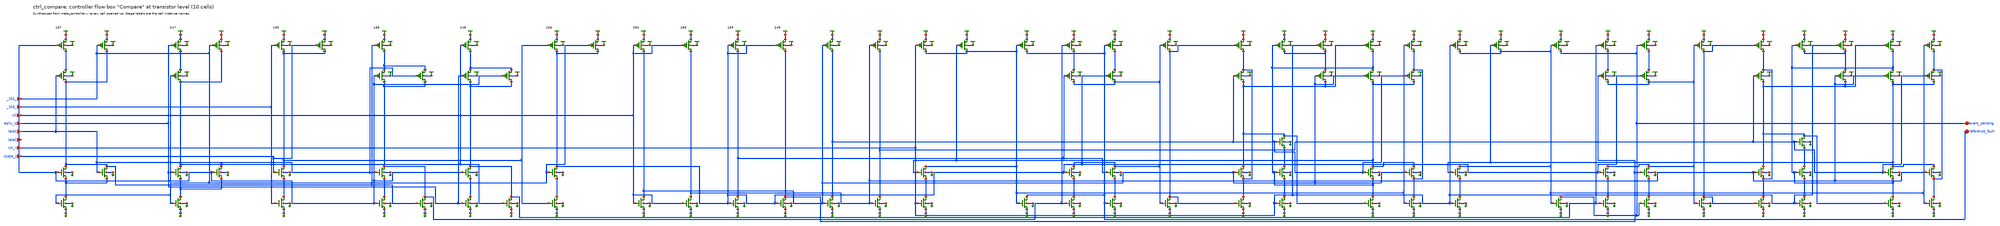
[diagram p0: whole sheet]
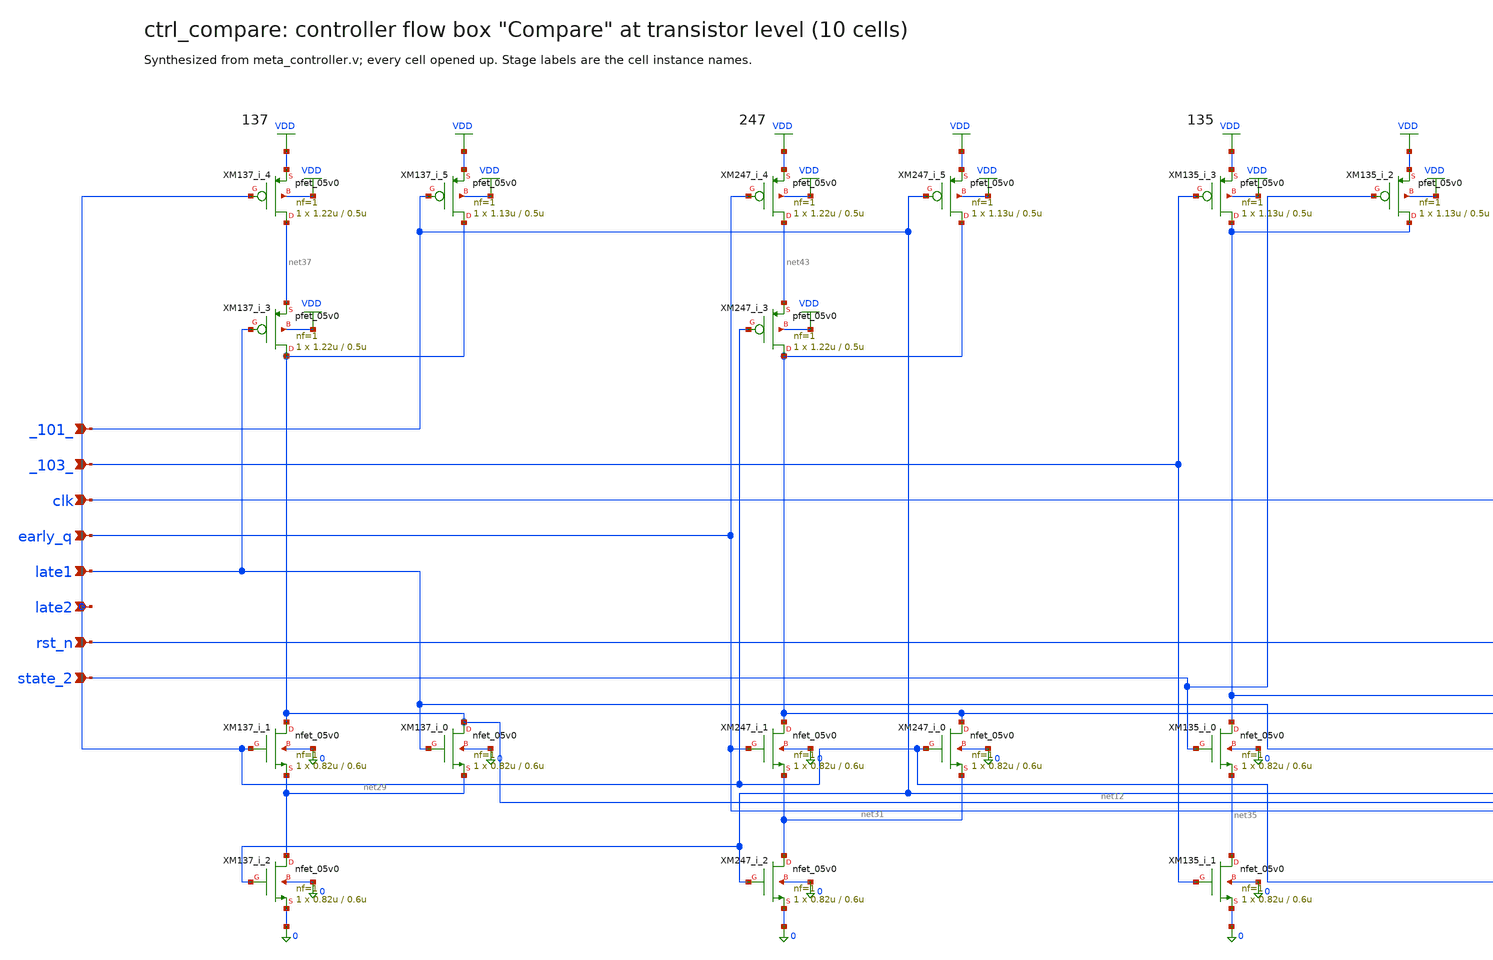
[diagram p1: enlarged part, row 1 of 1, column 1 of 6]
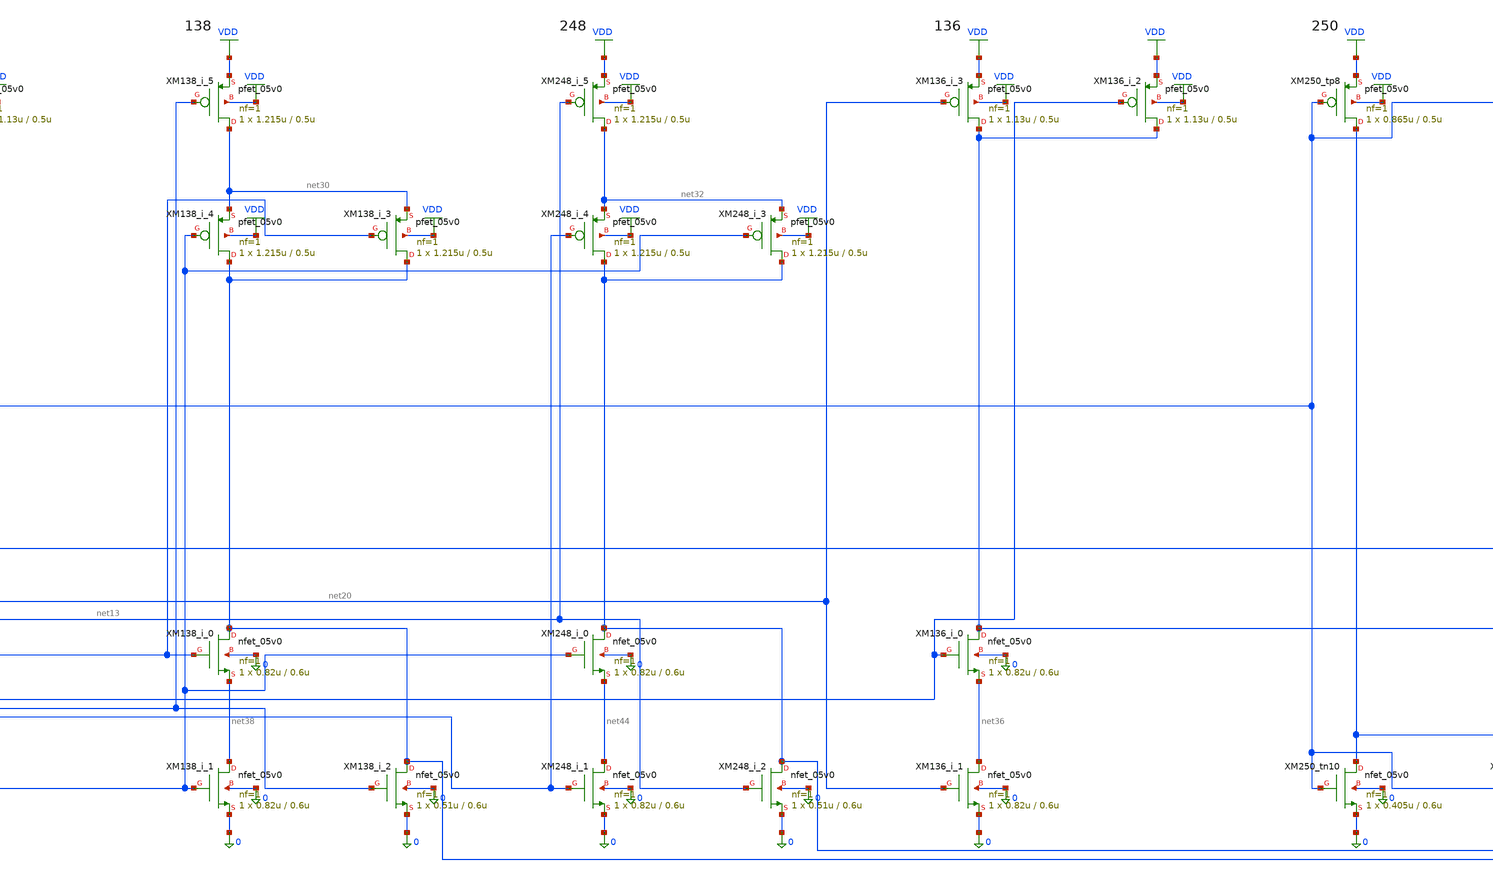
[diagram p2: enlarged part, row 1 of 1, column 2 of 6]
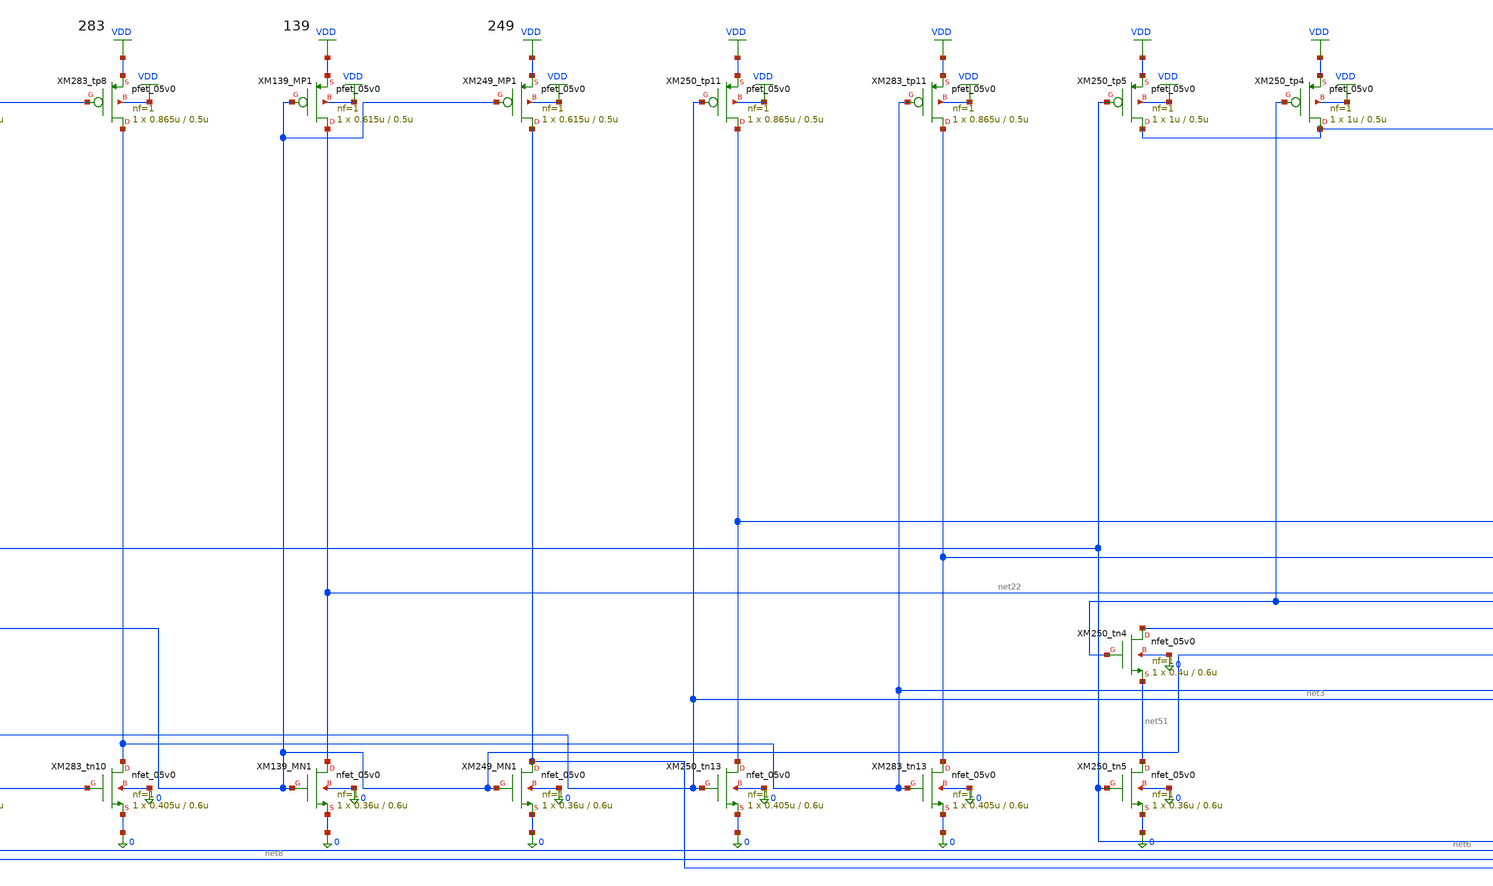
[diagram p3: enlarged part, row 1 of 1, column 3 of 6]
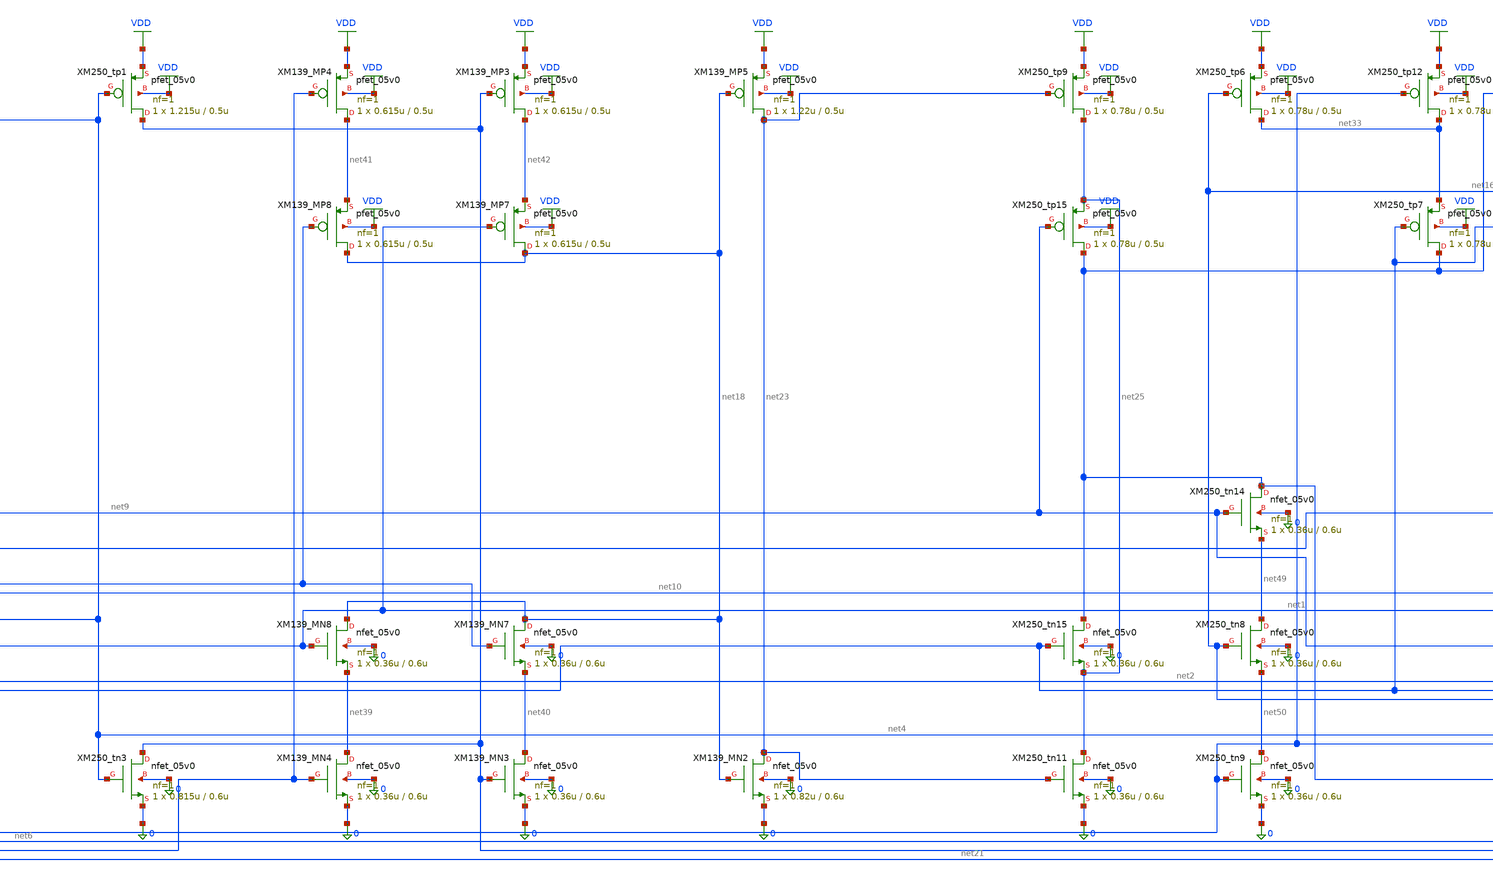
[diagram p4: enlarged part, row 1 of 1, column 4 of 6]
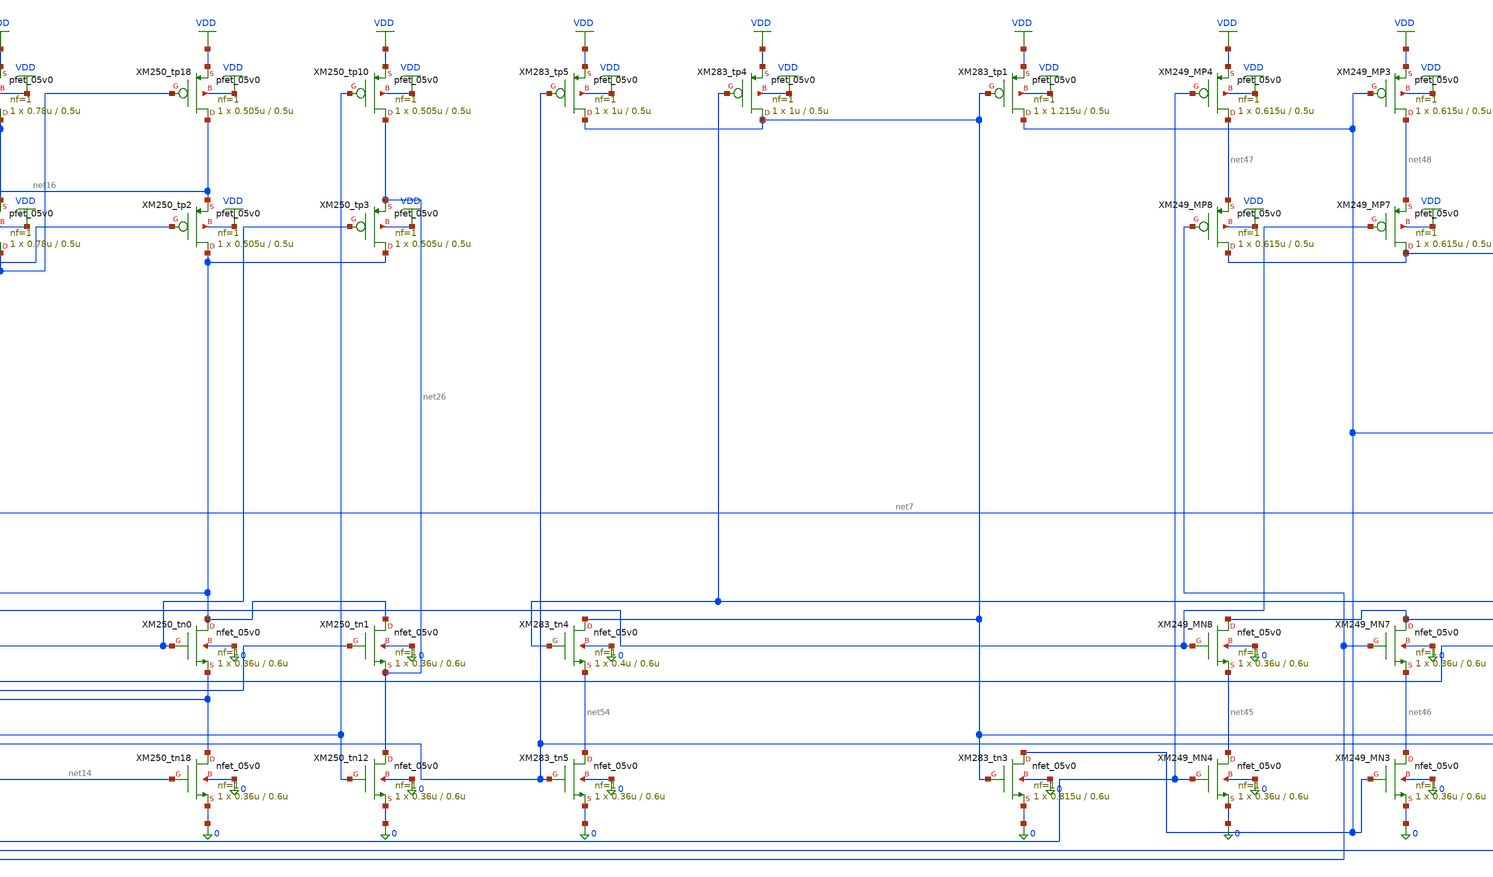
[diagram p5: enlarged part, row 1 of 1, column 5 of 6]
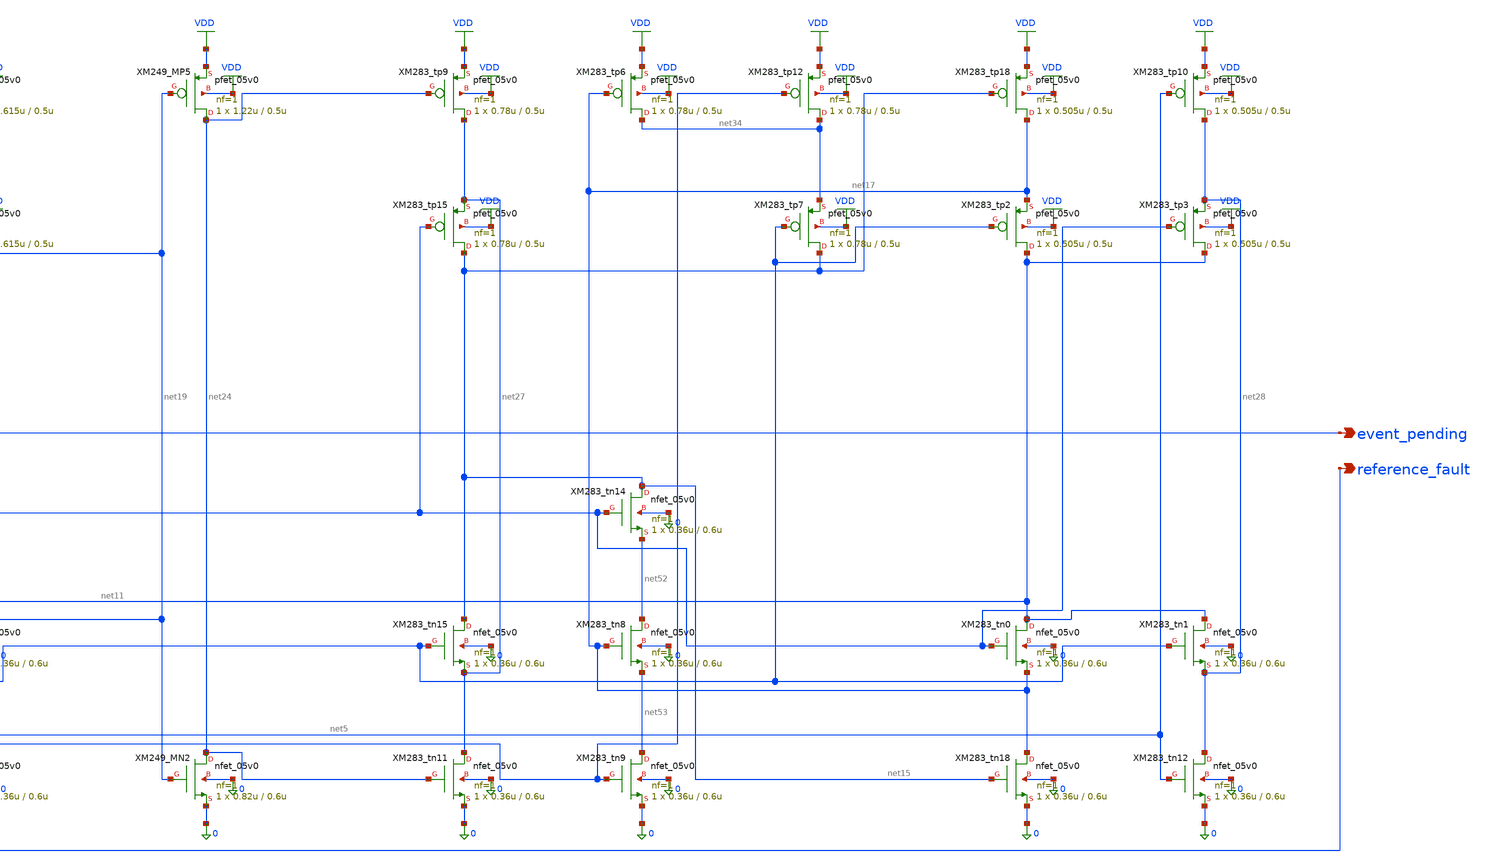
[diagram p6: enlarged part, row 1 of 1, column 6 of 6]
** sch_path: xschem/flat/ctrl_compare.sch
**.subckt ctrl_compare _101_ _103_ clk early_q late1 late2 rst_n state_2 event_pending
*+ reference_fault
*.ipin _101_
*.ipin _103_
*.ipin clk
*.ipin early_q
*.ipin late1
*.ipin late2
*.ipin rst_n
*.ipin state_2
*.opin event_pending
*.opin reference_fault
XM135_i_1 net35 _103_ 0 0 nfet_05v0 L=0.6u W=0.82u nf=1 ad=4.1e-13 as=4.1e-13 pd=2.64e-06
+ ps=2.64e-06 nrd=0 nrs=0 sa=0 sb=0 sd=0 m=1
XM135_i_0 net20 state_2 net35 0 nfet_05v0 L=0.6u W=0.82u nf=1 ad=4.1e-13 as=4.1e-13 pd=2.64e-06
+ ps=2.64e-06 nrd=0 nrs=0 sa=0 sb=0 sd=0 m=1
XM135_i_3 net20 _103_ VDD VDD pfet_05v0 L=0.5u W=1.13u nf=1 ad=5.65e-13 as=5.65e-13 pd=3.26e-06
+ ps=3.26e-06 nrd=0 nrs=0 sa=0 sb=0 sd=0 m=1
XM135_i_2 net20 state_2 VDD VDD pfet_05v0 L=0.5u W=1.13u nf=1 ad=5.65e-13 as=5.65e-13 pd=3.26e-06
+ ps=3.26e-06 nrd=0 nrs=0 sa=0 sb=0 sd=0 m=1
XM136_i_1 net36 net20 0 0 nfet_05v0 L=0.6u W=0.82u nf=1 ad=4.1e-13 as=4.1e-13 pd=2.64e-06
+ ps=2.64e-06 nrd=0 nrs=0 sa=0 sb=0 sd=0 m=1
XM136_i_0 net1 _101_ net36 0 nfet_05v0 L=0.6u W=0.82u nf=1 ad=4.1e-13 as=4.1e-13 pd=2.64e-06
+ ps=2.64e-06 nrd=0 nrs=0 sa=0 sb=0 sd=0 m=1
XM136_i_3 net1 net20 VDD VDD pfet_05v0 L=0.5u W=1.13u nf=1 ad=5.65e-13 as=5.65e-13 pd=3.26e-06
+ ps=3.26e-06 nrd=0 nrs=0 sa=0 sb=0 sd=0 m=1
XM136_i_2 net1 _101_ VDD VDD pfet_05v0 L=0.5u W=1.13u nf=1 ad=5.65e-13 as=5.65e-13 pd=3.26e-06
+ ps=3.26e-06 nrd=0 nrs=0 sa=0 sb=0 sd=0 m=1
XM137_i_1 net12 late2 net29 0 nfet_05v0 L=0.6u W=0.82u nf=1 ad=4.1e-13 as=4.1e-13 pd=2.64e-06
+ ps=2.64e-06 nrd=0 nrs=0 sa=0 sb=0 sd=0 m=1
XM137_i_0 net12 late1 net29 0 nfet_05v0 L=0.6u W=0.82u nf=1 ad=4.1e-13 as=4.1e-13 pd=2.64e-06
+ ps=2.64e-06 nrd=0 nrs=0 sa=0 sb=0 sd=0 m=1
XM137_i_2 net29 _101_ 0 0 nfet_05v0 L=0.6u W=0.82u nf=1 ad=4.1e-13 as=4.1e-13 pd=2.64e-06
+ ps=2.64e-06 nrd=0 nrs=0 sa=0 sb=0 sd=0 m=1
XM137_i_4 net37 late2 VDD VDD pfet_05v0 L=0.5u W=1.22u nf=1 ad=6.1e-13 as=6.1e-13 pd=3.44e-06
+ ps=3.44e-06 nrd=0 nrs=0 sa=0 sb=0 sd=0 m=1
XM137_i_3 net12 late1 net37 VDD pfet_05v0 L=0.5u W=1.22u nf=1 ad=6.1e-13 as=6.1e-13 pd=3.44e-06
+ ps=3.44e-06 nrd=0 nrs=0 sa=0 sb=0 sd=0 m=1
XM137_i_5 net12 _101_ VDD VDD pfet_05v0 L=0.5u W=1.13u nf=1 ad=5.65e-13 as=5.65e-13 pd=3.26e-06
+ ps=3.26e-06 nrd=0 nrs=0 sa=0 sb=0 sd=0 m=1
XM138_i_1 net38 late2 0 0 nfet_05v0 L=0.6u W=0.82u nf=1 ad=4.1e-13 as=4.1e-13 pd=2.64e-06
+ ps=2.64e-06 nrd=0 nrs=0 sa=0 sb=0 sd=0 m=1
XM138_i_0 net8 late1 net38 0 nfet_05v0 L=0.6u W=0.82u nf=1 ad=4.1e-13 as=4.1e-13 pd=2.64e-06
+ ps=2.64e-06 nrd=0 nrs=0 sa=0 sb=0 sd=0 m=1
XM138_i_2 net8 net12 0 0 nfet_05v0 L=0.6u W=0.51u nf=1 ad=2.55e-13 as=2.55e-13 pd=2.02e-06
+ ps=2.02e-06 nrd=0 nrs=0 sa=0 sb=0 sd=0 m=1
XM138_i_4 net8 late2 net30 VDD pfet_05v0 L=0.5u W=1.215u nf=1 ad=6.075e-13 as=6.075e-13 pd=3.43e-06
+ ps=3.43e-06 nrd=0 nrs=0 sa=0 sb=0 sd=0 m=1
XM138_i_3 net8 late1 net30 VDD pfet_05v0 L=0.5u W=1.215u nf=1 ad=6.075e-13 as=6.075e-13 pd=3.43e-06
+ ps=3.43e-06 nrd=0 nrs=0 sa=0 sb=0 sd=0 m=1
XM138_i_5 net30 net12 VDD VDD pfet_05v0 L=0.5u W=1.215u nf=1 ad=6.075e-13 as=6.075e-13 pd=3.43e-06
+ ps=3.43e-06 nrd=0 nrs=0 sa=0 sb=0 sd=0 m=1
XM139_MN2 net23 net18 0 0 nfet_05v0 L=0.6u W=0.82u nf=1 ad=4.1e-13 as=4.1e-13 pd=2.64e-06
+ ps=2.64e-06 nrd=0 nrs=0 sa=0 sb=0 sd=0 m=1
XM139_MN4 net39 net8 0 0 nfet_05v0 L=0.6u W=0.36u nf=1 ad=1.8e-13 as=1.8e-13 pd=1.72e-06 ps=1.72e-06
+ nrd=0 nrs=0 sa=0 sb=0 sd=0 m=1
XM139_MN8 net18 net1 net39 0 nfet_05v0 L=0.6u W=0.36u nf=1 ad=1.8e-13 as=1.8e-13 pd=1.72e-06
+ ps=1.72e-06 nrd=0 nrs=0 sa=0 sb=0 sd=0 m=1
XM139_MN7 net18 net22 net40 0 nfet_05v0 L=0.6u W=0.36u nf=1 ad=1.8e-13 as=1.8e-13 pd=1.72e-06
+ ps=1.72e-06 nrd=0 nrs=0 sa=0 sb=0 sd=0 m=1
XM139_MN3 net40 reference_fault 0 0 nfet_05v0 L=0.6u W=0.36u nf=1 ad=1.8e-13 as=1.8e-13 pd=1.72e-06
+ ps=1.72e-06 nrd=0 nrs=0 sa=0 sb=0 sd=0 m=1
XM139_MN1 net22 net1 0 0 nfet_05v0 L=0.6u W=0.36u nf=1 ad=1.8e-13 as=1.8e-13 pd=1.72e-06 ps=1.72e-06
+ nrd=0 nrs=0 sa=0 sb=0 sd=0 m=1
XM139_MP5 net23 net18 VDD VDD pfet_05v0 L=0.5u W=1.22u nf=1 ad=6.1e-13 as=6.1e-13 pd=3.44e-06
+ ps=3.44e-06 nrd=0 nrs=0 sa=0 sb=0 sd=0 m=1
XM139_MP4 net41 net8 VDD VDD pfet_05v0 L=0.5u W=0.615u nf=1 ad=3.075e-13 as=3.075e-13 pd=2.23e-06
+ ps=2.23e-06 nrd=0 nrs=0 sa=0 sb=0 sd=0 m=1
XM139_MP8 net18 net22 net41 VDD pfet_05v0 L=0.5u W=0.615u nf=1 ad=3.075e-13 as=3.075e-13 pd=2.23e-06
+ ps=2.23e-06 nrd=0 nrs=0 sa=0 sb=0 sd=0 m=1
XM139_MP7 net18 net1 net42 VDD pfet_05v0 L=0.5u W=0.615u nf=1 ad=3.075e-13 as=3.075e-13 pd=2.23e-06
+ ps=2.23e-06 nrd=0 nrs=0 sa=0 sb=0 sd=0 m=1
XM139_MP3 net42 reference_fault VDD VDD pfet_05v0 L=0.5u W=0.615u nf=1 ad=3.075e-13 as=3.075e-13
+ pd=2.23e-06 ps=2.23e-06 nrd=0 nrs=0 sa=0 sb=0 sd=0 m=1
XM139_MP1 net22 net1 VDD VDD pfet_05v0 L=0.5u W=0.615u nf=1 ad=3.075e-13 as=3.075e-13 pd=2.23e-06
+ ps=2.23e-06 nrd=0 nrs=0 sa=0 sb=0 sd=0 m=1
XM247_i_1 net13 early_q net31 0 nfet_05v0 L=0.6u W=0.82u nf=1 ad=4.1e-13 as=4.1e-13 pd=2.64e-06
+ ps=2.64e-06 nrd=0 nrs=0 sa=0 sb=0 sd=0 m=1
XM247_i_0 net13 late2 net31 0 nfet_05v0 L=0.6u W=0.82u nf=1 ad=4.1e-13 as=4.1e-13 pd=2.64e-06
+ ps=2.64e-06 nrd=0 nrs=0 sa=0 sb=0 sd=0 m=1
XM247_i_2 net31 _101_ 0 0 nfet_05v0 L=0.6u W=0.82u nf=1 ad=4.1e-13 as=4.1e-13 pd=2.64e-06
+ ps=2.64e-06 nrd=0 nrs=0 sa=0 sb=0 sd=0 m=1
XM247_i_4 net43 early_q VDD VDD pfet_05v0 L=0.5u W=1.22u nf=1 ad=6.1e-13 as=6.1e-13 pd=3.44e-06
+ ps=3.44e-06 nrd=0 nrs=0 sa=0 sb=0 sd=0 m=1
XM247_i_3 net13 late2 net43 VDD pfet_05v0 L=0.5u W=1.22u nf=1 ad=6.1e-13 as=6.1e-13 pd=3.44e-06
+ ps=3.44e-06 nrd=0 nrs=0 sa=0 sb=0 sd=0 m=1
XM247_i_5 net13 _101_ VDD VDD pfet_05v0 L=0.5u W=1.13u nf=1 ad=5.65e-13 as=5.65e-13 pd=3.26e-06
+ ps=3.26e-06 nrd=0 nrs=0 sa=0 sb=0 sd=0 m=1
XM248_i_1 net44 early_q 0 0 nfet_05v0 L=0.6u W=0.82u nf=1 ad=4.1e-13 as=4.1e-13 pd=2.64e-06
+ ps=2.64e-06 nrd=0 nrs=0 sa=0 sb=0 sd=0 m=1
XM248_i_0 net6 late2 net44 0 nfet_05v0 L=0.6u W=0.82u nf=1 ad=4.1e-13 as=4.1e-13 pd=2.64e-06
+ ps=2.64e-06 nrd=0 nrs=0 sa=0 sb=0 sd=0 m=1
XM248_i_2 net6 net13 0 0 nfet_05v0 L=0.6u W=0.51u nf=1 ad=2.55e-13 as=2.55e-13 pd=2.02e-06
+ ps=2.02e-06 nrd=0 nrs=0 sa=0 sb=0 sd=0 m=1
XM248_i_4 net6 early_q net32 VDD pfet_05v0 L=0.5u W=1.215u nf=1 ad=6.075e-13 as=6.075e-13
+ pd=3.43e-06 ps=3.43e-06 nrd=0 nrs=0 sa=0 sb=0 sd=0 m=1
XM248_i_3 net6 late2 net32 VDD pfet_05v0 L=0.5u W=1.215u nf=1 ad=6.075e-13 as=6.075e-13 pd=3.43e-06
+ ps=3.43e-06 nrd=0 nrs=0 sa=0 sb=0 sd=0 m=1
XM248_i_5 net32 net13 VDD VDD pfet_05v0 L=0.5u W=1.215u nf=1 ad=6.075e-13 as=6.075e-13 pd=3.43e-06
+ ps=3.43e-06 nrd=0 nrs=0 sa=0 sb=0 sd=0 m=1
XM249_MN2 net24 net19 0 0 nfet_05v0 L=0.6u W=0.82u nf=1 ad=4.1e-13 as=4.1e-13 pd=2.64e-06
+ ps=2.64e-06 nrd=0 nrs=0 sa=0 sb=0 sd=0 m=1
XM249_MN4 net45 net6 0 0 nfet_05v0 L=0.6u W=0.36u nf=1 ad=1.8e-13 as=1.8e-13 pd=1.72e-06 ps=1.72e-06
+ nrd=0 nrs=0 sa=0 sb=0 sd=0 m=1
XM249_MN8 net19 net1 net45 0 nfet_05v0 L=0.6u W=0.36u nf=1 ad=1.8e-13 as=1.8e-13 pd=1.72e-06
+ ps=1.72e-06 nrd=0 nrs=0 sa=0 sb=0 sd=0 m=1
XM249_MN7 net19 net21 net46 0 nfet_05v0 L=0.6u W=0.36u nf=1 ad=1.8e-13 as=1.8e-13 pd=1.72e-06
+ ps=1.72e-06 nrd=0 nrs=0 sa=0 sb=0 sd=0 m=1
XM249_MN3 net46 event_pending 0 0 nfet_05v0 L=0.6u W=0.36u nf=1 ad=1.8e-13 as=1.8e-13 pd=1.72e-06
+ ps=1.72e-06 nrd=0 nrs=0 sa=0 sb=0 sd=0 m=1
XM249_MN1 net21 net1 0 0 nfet_05v0 L=0.6u W=0.36u nf=1 ad=1.8e-13 as=1.8e-13 pd=1.72e-06 ps=1.72e-06
+ nrd=0 nrs=0 sa=0 sb=0 sd=0 m=1
XM249_MP5 net24 net19 VDD VDD pfet_05v0 L=0.5u W=1.22u nf=1 ad=6.1e-13 as=6.1e-13 pd=3.44e-06
+ ps=3.44e-06 nrd=0 nrs=0 sa=0 sb=0 sd=0 m=1
XM249_MP4 net47 net6 VDD VDD pfet_05v0 L=0.5u W=0.615u nf=1 ad=3.075e-13 as=3.075e-13 pd=2.23e-06
+ ps=2.23e-06 nrd=0 nrs=0 sa=0 sb=0 sd=0 m=1
XM249_MP8 net19 net21 net47 VDD pfet_05v0 L=0.5u W=0.615u nf=1 ad=3.075e-13 as=3.075e-13 pd=2.23e-06
+ ps=2.23e-06 nrd=0 nrs=0 sa=0 sb=0 sd=0 m=1
XM249_MP7 net19 net1 net48 VDD pfet_05v0 L=0.5u W=0.615u nf=1 ad=3.075e-13 as=3.075e-13 pd=2.23e-06
+ ps=2.23e-06 nrd=0 nrs=0 sa=0 sb=0 sd=0 m=1
XM249_MP3 net48 event_pending VDD VDD pfet_05v0 L=0.5u W=0.615u nf=1 ad=3.075e-13 as=3.075e-13
+ pd=2.23e-06 ps=2.23e-06 nrd=0 nrs=0 sa=0 sb=0 sd=0 m=1
XM249_MP1 net21 net1 VDD VDD pfet_05v0 L=0.5u W=0.615u nf=1 ad=3.075e-13 as=3.075e-13 pd=2.23e-06
+ ps=2.23e-06 nrd=0 nrs=0 sa=0 sb=0 sd=0 m=1
XM250_tn10 net3 clk 0 0 nfet_05v0 L=0.6u W=0.405u nf=1 ad=2.025e-13 as=2.025e-13 pd=1.81e-06
+ ps=1.81e-06 nrd=0 nrs=0 sa=0 sb=0 sd=0 m=1
XM250_tn13 net9 net3 0 0 nfet_05v0 L=0.6u W=0.405u nf=1 ad=2.025e-13 as=2.025e-13 pd=1.81e-06
+ ps=1.81e-06 nrd=0 nrs=0 sa=0 sb=0 sd=0 m=1
XM250_tn11 net25 net23 0 0 nfet_05v0 L=0.6u W=0.36u nf=1 ad=1.8e-13 as=1.8e-13 pd=1.72e-06
+ ps=1.72e-06 nrd=0 nrs=0 sa=0 sb=0 sd=0 m=1
XM250_tn15 net14 net3 net25 0 nfet_05v0 L=0.6u W=0.36u nf=1 ad=1.8e-13 as=1.8e-13 pd=1.72e-06
+ ps=1.72e-06 nrd=0 nrs=0 sa=0 sb=0 sd=0 m=1
XM250_tn14 net14 net9 net49 0 nfet_05v0 L=0.6u W=0.36u nf=1 ad=1.8e-13 as=1.8e-13 pd=1.72e-06
+ ps=1.72e-06 nrd=0 nrs=0 sa=0 sb=0 sd=0 m=1
XM250_tn8 net49 net16 net50 0 nfet_05v0 L=0.6u W=0.36u nf=1 ad=1.8e-13 as=1.8e-13 pd=1.72e-06
+ ps=1.72e-06 nrd=0 nrs=0 sa=0 sb=0 sd=0 m=1
XM250_tn9 net50 rst_n 0 0 nfet_05v0 L=0.6u W=0.36u nf=1 ad=1.8e-13 as=1.8e-13 pd=1.72e-06
+ ps=1.72e-06 nrd=0 nrs=0 sa=0 sb=0 sd=0 m=1
XM250_tn18 net16 net14 0 0 nfet_05v0 L=0.6u W=0.36u nf=1 ad=1.8e-13 as=1.8e-13 pd=1.72e-06
+ ps=1.72e-06 nrd=0 nrs=0 sa=0 sb=0 sd=0 m=1
XM250_tn0 net10 net9 net16 0 nfet_05v0 L=0.6u W=0.36u nf=1 ad=1.8e-13 as=1.8e-13 pd=1.72e-06
+ ps=1.72e-06 nrd=0 nrs=0 sa=0 sb=0 sd=0 m=1
XM250_tn1 net10 net3 net26 0 nfet_05v0 L=0.6u W=0.36u nf=1 ad=1.8e-13 as=1.8e-13 pd=1.72e-06
+ ps=1.72e-06 nrd=0 nrs=0 sa=0 sb=0 sd=0 m=1
XM250_tn12 net26 net4 0 0 nfet_05v0 L=0.6u W=0.36u nf=1 ad=1.8e-13 as=1.8e-13 pd=1.72e-06
+ ps=1.72e-06 nrd=0 nrs=0 sa=0 sb=0 sd=0 m=1
XM250_tn5 net51 rst_n 0 0 nfet_05v0 L=0.6u W=0.36u nf=1 ad=1.8e-13 as=1.8e-13 pd=1.72e-06
+ ps=1.72e-06 nrd=0 nrs=0 sa=0 sb=0 sd=0 m=1
XM250_tn4 net4 net10 net51 0 nfet_05v0 L=0.6u W=0.4u nf=1 ad=2e-13 as=2e-13 pd=1.8e-06 ps=1.8e-06
+ nrd=0 nrs=0 sa=0 sb=0 sd=0 m=1
XM250_tn3 reference_fault net4 0 0 nfet_05v0 L=0.6u W=0.815u nf=1 ad=4.075e-13 as=4.075e-13
+ pd=2.63e-06 ps=2.63e-06 nrd=0 nrs=0 sa=0 sb=0 sd=0 m=1
XM250_tp8 net3 clk VDD VDD pfet_05v0 L=0.5u W=0.865u nf=1 ad=4.325e-13 as=4.325e-13 pd=2.73e-06
+ ps=2.73e-06 nrd=0 nrs=0 sa=0 sb=0 sd=0 m=1
XM250_tp11 net9 net3 VDD VDD pfet_05v0 L=0.5u W=0.865u nf=1 ad=4.325e-13 as=4.325e-13 pd=2.73e-06
+ ps=2.73e-06 nrd=0 nrs=0 sa=0 sb=0 sd=0 m=1
XM250_tp9 net25 net23 VDD VDD pfet_05v0 L=0.5u W=0.78u nf=1 ad=3.9e-13 as=3.9e-13 pd=2.56e-06
+ ps=2.56e-06 nrd=0 nrs=0 sa=0 sb=0 sd=0 m=1
XM250_tp15 net14 net9 net25 VDD pfet_05v0 L=0.5u W=0.78u nf=1 ad=3.9e-13 as=3.9e-13 pd=2.56e-06
+ ps=2.56e-06 nrd=0 nrs=0 sa=0 sb=0 sd=0 m=1
XM250_tp7 net14 net3 net33 VDD pfet_05v0 L=0.5u W=0.78u nf=1 ad=3.9e-13 as=3.9e-13 pd=2.56e-06
+ ps=2.56e-06 nrd=0 nrs=0 sa=0 sb=0 sd=0 m=1
XM250_tp6 net33 net16 VDD VDD pfet_05v0 L=0.5u W=0.78u nf=1 ad=3.9e-13 as=3.9e-13 pd=2.56e-06
+ ps=2.56e-06 nrd=0 nrs=0 sa=0 sb=0 sd=0 m=1
XM250_tp12 net33 rst_n VDD VDD pfet_05v0 L=0.5u W=0.78u nf=1 ad=3.9e-13 as=3.9e-13 pd=2.56e-06
+ ps=2.56e-06 nrd=0 nrs=0 sa=0 sb=0 sd=0 m=1
XM250_tp18 net16 net14 VDD VDD pfet_05v0 L=0.5u W=0.505u nf=1 ad=2.525e-13 as=2.525e-13 pd=2.01e-06
+ ps=2.01e-06 nrd=0 nrs=0 sa=0 sb=0 sd=0 m=1
XM250_tp2 net10 net3 net16 VDD pfet_05v0 L=0.5u W=0.505u nf=1 ad=2.525e-13 as=2.525e-13 pd=2.01e-06
+ ps=2.01e-06 nrd=0 nrs=0 sa=0 sb=0 sd=0 m=1
XM250_tp3 net10 net9 net26 VDD pfet_05v0 L=0.5u W=0.505u nf=1 ad=2.525e-13 as=2.525e-13 pd=2.01e-06
+ ps=2.01e-06 nrd=0 nrs=0 sa=0 sb=0 sd=0 m=1
XM250_tp10 net26 net4 VDD VDD pfet_05v0 L=0.5u W=0.505u nf=1 ad=2.525e-13 as=2.525e-13 pd=2.01e-06
+ ps=2.01e-06 nrd=0 nrs=0 sa=0 sb=0 sd=0 m=1
XM250_tp5 net4 rst_n VDD VDD pfet_05v0 L=0.5u W=1u nf=1 ad=5e-13 as=5e-13 pd=3e-06 ps=3e-06 nrd=0
+ nrs=0 sa=0 sb=0 sd=0 m=1
XM250_tp4 net4 net10 VDD VDD pfet_05v0 L=0.5u W=1u nf=1 ad=5e-13 as=5e-13 pd=3e-06 ps=3e-06 nrd=0
+ nrs=0 sa=0 sb=0 sd=0 m=1
XM250_tp1 reference_fault net4 VDD VDD pfet_05v0 L=0.5u W=1.215u nf=1 ad=6.075e-13 as=6.075e-13
+ pd=3.43e-06 ps=3.43e-06 nrd=0 nrs=0 sa=0 sb=0 sd=0 m=1
XM283_tn10 net2 clk 0 0 nfet_05v0 L=0.6u W=0.405u nf=1 ad=2.025e-13 as=2.025e-13 pd=1.81e-06
+ ps=1.81e-06 nrd=0 nrs=0 sa=0 sb=0 sd=0 m=1
XM283_tn13 net7 net2 0 0 nfet_05v0 L=0.6u W=0.405u nf=1 ad=2.025e-13 as=2.025e-13 pd=1.81e-06
+ ps=1.81e-06 nrd=0 nrs=0 sa=0 sb=0 sd=0 m=1
XM283_tn11 net27 net24 0 0 nfet_05v0 L=0.6u W=0.36u nf=1 ad=1.8e-13 as=1.8e-13 pd=1.72e-06
+ ps=1.72e-06 nrd=0 nrs=0 sa=0 sb=0 sd=0 m=1
XM283_tn15 net15 net2 net27 0 nfet_05v0 L=0.6u W=0.36u nf=1 ad=1.8e-13 as=1.8e-13 pd=1.72e-06
+ ps=1.72e-06 nrd=0 nrs=0 sa=0 sb=0 sd=0 m=1
XM283_tn14 net15 net7 net52 0 nfet_05v0 L=0.6u W=0.36u nf=1 ad=1.8e-13 as=1.8e-13 pd=1.72e-06
+ ps=1.72e-06 nrd=0 nrs=0 sa=0 sb=0 sd=0 m=1
XM283_tn8 net52 net17 net53 0 nfet_05v0 L=0.6u W=0.36u nf=1 ad=1.8e-13 as=1.8e-13 pd=1.72e-06
+ ps=1.72e-06 nrd=0 nrs=0 sa=0 sb=0 sd=0 m=1
XM283_tn9 net53 rst_n 0 0 nfet_05v0 L=0.6u W=0.36u nf=1 ad=1.8e-13 as=1.8e-13 pd=1.72e-06
+ ps=1.72e-06 nrd=0 nrs=0 sa=0 sb=0 sd=0 m=1
XM283_tn18 net17 net15 0 0 nfet_05v0 L=0.6u W=0.36u nf=1 ad=1.8e-13 as=1.8e-13 pd=1.72e-06
+ ps=1.72e-06 nrd=0 nrs=0 sa=0 sb=0 sd=0 m=1
XM283_tn0 net11 net7 net17 0 nfet_05v0 L=0.6u W=0.36u nf=1 ad=1.8e-13 as=1.8e-13 pd=1.72e-06
+ ps=1.72e-06 nrd=0 nrs=0 sa=0 sb=0 sd=0 m=1
XM283_tn1 net11 net2 net28 0 nfet_05v0 L=0.6u W=0.36u nf=1 ad=1.8e-13 as=1.8e-13 pd=1.72e-06
+ ps=1.72e-06 nrd=0 nrs=0 sa=0 sb=0 sd=0 m=1
XM283_tn12 net28 net5 0 0 nfet_05v0 L=0.6u W=0.36u nf=1 ad=1.8e-13 as=1.8e-13 pd=1.72e-06
+ ps=1.72e-06 nrd=0 nrs=0 sa=0 sb=0 sd=0 m=1
XM283_tn5 net54 rst_n 0 0 nfet_05v0 L=0.6u W=0.36u nf=1 ad=1.8e-13 as=1.8e-13 pd=1.72e-06
+ ps=1.72e-06 nrd=0 nrs=0 sa=0 sb=0 sd=0 m=1
XM283_tn4 net5 net11 net54 0 nfet_05v0 L=0.6u W=0.4u nf=1 ad=2e-13 as=2e-13 pd=1.8e-06 ps=1.8e-06
+ nrd=0 nrs=0 sa=0 sb=0 sd=0 m=1
XM283_tn3 event_pending net5 0 0 nfet_05v0 L=0.6u W=0.815u nf=1 ad=4.075e-13 as=4.075e-13
+ pd=2.63e-06 ps=2.63e-06 nrd=0 nrs=0 sa=0 sb=0 sd=0 m=1
XM283_tp8 net2 clk VDD VDD pfet_05v0 L=0.5u W=0.865u nf=1 ad=4.325e-13 as=4.325e-13 pd=2.73e-06
+ ps=2.73e-06 nrd=0 nrs=0 sa=0 sb=0 sd=0 m=1
XM283_tp11 net7 net2 VDD VDD pfet_05v0 L=0.5u W=0.865u nf=1 ad=4.325e-13 as=4.325e-13 pd=2.73e-06
+ ps=2.73e-06 nrd=0 nrs=0 sa=0 sb=0 sd=0 m=1
XM283_tp9 net27 net24 VDD VDD pfet_05v0 L=0.5u W=0.78u nf=1 ad=3.9e-13 as=3.9e-13 pd=2.56e-06
+ ps=2.56e-06 nrd=0 nrs=0 sa=0 sb=0 sd=0 m=1
XM283_tp15 net15 net7 net27 VDD pfet_05v0 L=0.5u W=0.78u nf=1 ad=3.9e-13 as=3.9e-13 pd=2.56e-06
+ ps=2.56e-06 nrd=0 nrs=0 sa=0 sb=0 sd=0 m=1
XM283_tp7 net15 net2 net34 VDD pfet_05v0 L=0.5u W=0.78u nf=1 ad=3.9e-13 as=3.9e-13 pd=2.56e-06
+ ps=2.56e-06 nrd=0 nrs=0 sa=0 sb=0 sd=0 m=1
XM283_tp6 net34 net17 VDD VDD pfet_05v0 L=0.5u W=0.78u nf=1 ad=3.9e-13 as=3.9e-13 pd=2.56e-06
+ ps=2.56e-06 nrd=0 nrs=0 sa=0 sb=0 sd=0 m=1
XM283_tp12 net34 rst_n VDD VDD pfet_05v0 L=0.5u W=0.78u nf=1 ad=3.9e-13 as=3.9e-13 pd=2.56e-06
+ ps=2.56e-06 nrd=0 nrs=0 sa=0 sb=0 sd=0 m=1
XM283_tp18 net17 net15 VDD VDD pfet_05v0 L=0.5u W=0.505u nf=1 ad=2.525e-13 as=2.525e-13 pd=2.01e-06
+ ps=2.01e-06 nrd=0 nrs=0 sa=0 sb=0 sd=0 m=1
XM283_tp2 net11 net2 net17 VDD pfet_05v0 L=0.5u W=0.505u nf=1 ad=2.525e-13 as=2.525e-13 pd=2.01e-06
+ ps=2.01e-06 nrd=0 nrs=0 sa=0 sb=0 sd=0 m=1
XM283_tp3 net11 net7 net28 VDD pfet_05v0 L=0.5u W=0.505u nf=1 ad=2.525e-13 as=2.525e-13 pd=2.01e-06
+ ps=2.01e-06 nrd=0 nrs=0 sa=0 sb=0 sd=0 m=1
XM283_tp10 net28 net5 VDD VDD pfet_05v0 L=0.5u W=0.505u nf=1 ad=2.525e-13 as=2.525e-13 pd=2.01e-06
+ ps=2.01e-06 nrd=0 nrs=0 sa=0 sb=0 sd=0 m=1
XM283_tp5 net5 rst_n VDD VDD pfet_05v0 L=0.5u W=1u nf=1 ad=5e-13 as=5e-13 pd=3e-06 ps=3e-06 nrd=0
+ nrs=0 sa=0 sb=0 sd=0 m=1
XM283_tp4 net5 net11 VDD VDD pfet_05v0 L=0.5u W=1u nf=1 ad=5e-13 as=5e-13 pd=3e-06 ps=3e-06 nrd=0
+ nrs=0 sa=0 sb=0 sd=0 m=1
XM283_tp1 event_pending net5 VDD VDD pfet_05v0 L=0.5u W=1.215u nf=1 ad=6.075e-13 as=6.075e-13
+ pd=3.43e-06 ps=3.43e-06 nrd=0 nrs=0 sa=0 sb=0 sd=0 m=1
**.ends
.GLOBAL VDD
.end
